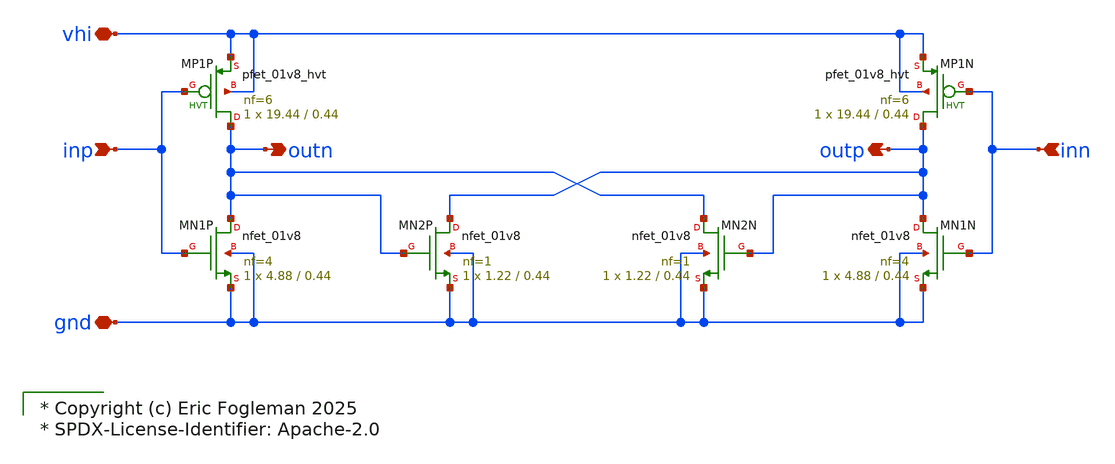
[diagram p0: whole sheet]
** sch_path: xschem/ejf_pll96_vco_dlycell.sch

* Copyright (c) Eric Fogleman 2025
* SPDX-License-Identifier: Apache-2.0

**.subckt ejf_pll96_vco_dlycell inp outn inn outp vhi gnd
*.ipin inp
*.opin outn
*.ipin inn
*.opin outp
*.iopin vhi
*.iopin gnd
XMN2P outp outn gnd gnd sky130_fd_pr__nfet_01v8 L=0.44 W=1.22 nf=1 ad='int((nf+1)/2) * W/nf * 0.29' as='int((nf+2)/2) * W/nf * 0.29'
+ pd='2*int((nf+1)/2) * (W/nf + 0.29)' ps='2*int((nf+2)/2) * (W/nf + 0.29)' nrd='0.29 / W' nrs='0.29 / W'
+ sa=0 sb=0 sd=0 mult=1 m=1
XMN1P outn inp gnd gnd sky130_fd_pr__nfet_01v8 L=0.44 W=4.88 nf=4 ad='int((nf+1)/2) * W/nf * 0.29' as='int((nf+2)/2) * W/nf * 0.29'
+ pd='2*int((nf+1)/2) * (W/nf + 0.29)' ps='2*int((nf+2)/2) * (W/nf + 0.29)' nrd='0.29 / W' nrs='0.29 / W'
+ sa=0 sb=0 sd=0 mult=1 m=1
XMP1P outn inp vhi vhi sky130_fd_pr__pfet_01v8_hvt L=0.44 W=19.44 nf=6 ad='int((nf+1)/2) * W/nf * 0.29'
+ as='int((nf+2)/2) * W/nf * 0.29' pd='2*int((nf+1)/2) * (W/nf + 0.29)' ps='2*int((nf+2)/2) * (W/nf + 0.29)'
+ nrd='0.29 / W' nrs='0.29 / W' sa=0 sb=0 sd=0 mult=1 m=1
XMN2N outn outp gnd gnd sky130_fd_pr__nfet_01v8 L=0.44 W=1.22 nf=1 ad='int((nf+1)/2) * W/nf * 0.29' as='int((nf+2)/2) * W/nf * 0.29'
+ pd='2*int((nf+1)/2) * (W/nf + 0.29)' ps='2*int((nf+2)/2) * (W/nf + 0.29)' nrd='0.29 / W' nrs='0.29 / W'
+ sa=0 sb=0 sd=0 mult=1 m=1
XMN1N outp inn gnd gnd sky130_fd_pr__nfet_01v8 L=0.44 W=4.88 nf=4 ad='int((nf+1)/2) * W/nf * 0.29' as='int((nf+2)/2) * W/nf * 0.29'
+ pd='2*int((nf+1)/2) * (W/nf + 0.29)' ps='2*int((nf+2)/2) * (W/nf + 0.29)' nrd='0.29 / W' nrs='0.29 / W'
+ sa=0 sb=0 sd=0 mult=1 m=1
XMP1N outp inn vhi vhi sky130_fd_pr__pfet_01v8_hvt L=0.44 W=19.44 nf=6 ad='int((nf+1)/2) * W/nf * 0.29'
+ as='int((nf+2)/2) * W/nf * 0.29' pd='2*int((nf+1)/2) * (W/nf + 0.29)' ps='2*int((nf+2)/2) * (W/nf + 0.29)'
+ nrd='0.29 / W' nrs='0.29 / W' sa=0 sb=0 sd=0 mult=1 m=1
**.ends
.end
